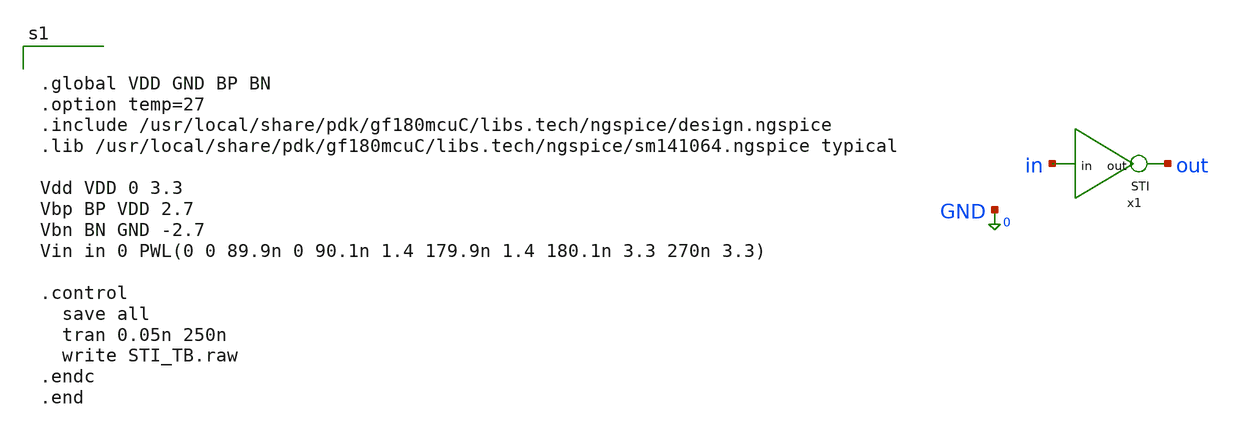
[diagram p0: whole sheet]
** sch_path: xschem_designs/STI_TB.sch
**.subckt STI_TB
x1 out in STI
**** begin user architecture code


.global VDD GND BP BN
.option temp=27
.include /usr/local/share/pdk/gf180mcuC/libs.tech/ngspice/design.ngspice
.lib /usr/local/share/pdk/gf180mcuC/libs.tech/ngspice/sm141064.ngspice typical

Vdd VDD 0 3.3
Vbp BP VDD 2.7
Vbn BN GND -2.7
Vin in 0 PWL(0 0 89.9n 0 90.1n 1.4 179.9n 1.4 180.1n 3.3 270n 3.3)

.control
  save all
  tran 0.05n 250n
  write STI_TB.raw
.endc
.end


**** end user architecture code
**.ends

* expanding   symbol:  xschem_designs/STI.sym # of pins=2
** sym_path: xschem_designs/STI.sym
** sch_path: xschem_designs/STI.sch
.subckt STI out in
*.ipin in
*.opin out
XM225 out out net1 GND nfet_03v3 L=2.24u W=0.22u nf=1 ad='int((nf+1)/2) * W/nf * 0.18u' as='int((nf+2)/2) * W/nf * 0.18u'
+ pd='2*int((nf+1)/2) * (W/nf + 0.18u)' ps='2*int((nf+2)/2) * (W/nf + 0.18u)' nrd='0.18u / W' nrs='0.18u / W'
+ sa=0 sb=0 sd=0 m=1 par=1
XM226 out out net2 VDD pfet_03v3 L=1.12u W=0.22u nf=1 ad='int((nf+1)/2) * W/nf * 0.18u' as='int((nf+2)/2) * W/nf * 0.18u'
+ pd='2*int((nf+1)/2) * (W/nf + 0.18u)' ps='2*int((nf+2)/2) * (W/nf + 0.18u)' nrd='0.18u / W' nrs='0.18u / W'
+ sa=0 sb=0 sd=0 m=1 par=1
XM237 net2 in VDD VDD pfet_03v3 L=0.28u W=0.44u nf=1 ad='int((nf+1)/2) * W/nf * 0.18u' as='int((nf+2)/2) * W/nf * 0.18u'
+ pd='2*int((nf+1)/2) * (W/nf + 0.18u)' ps='2*int((nf+2)/2) * (W/nf + 0.18u)' nrd='0.18u / W' nrs='0.18u / W'
+ sa=0 sb=0 sd=0 m=1 par=1
XM238 net1 in GND GND nfet_03v3 L=0.28u W=0.22u nf=1 ad='int((nf+1)/2) * W/nf * 0.18u' as='int((nf+2)/2) * W/nf * 0.18u'
+ pd='2*int((nf+1)/2) * (W/nf + 0.18u)' ps='2*int((nf+2)/2) * (W/nf + 0.18u)' nrd='0.18u / W' nrs='0.18u / W'
+ sa=0 sb=0 sd=0 m=1 par=1
XM241 out in VDD BP pfet_06v0 L=1.1u W=0.60u nf=1 ad='int((nf+1)/2) * W/nf * 0.18u' as='int((nf+2)/2) * W/nf * 0.18u'
+ pd='2*int((nf+1)/2) * (W/nf + 0.18u)' ps='2*int((nf+2)/2) * (W/nf + 0.18u)' nrd='0.18u / W' nrs='0.18u / W'
+ sa=0 sb=0 sd=0 m=1 par=1
XM242 out in GND BN nfet_06v0 L=1.4u W=0.30u nf=1 ad='int((nf+1)/2) * W/nf * 0.18u' as='int((nf+2)/2) * W/nf * 0.18u'
+ pd='2*int((nf+1)/2) * (W/nf + 0.18u)' ps='2*int((nf+2)/2) * (W/nf + 0.18u)' nrd='0.18u / W' nrs='0.18u / W'
+ sa=0 sb=0 sd=0 m=1 par=1
.ends

.end
